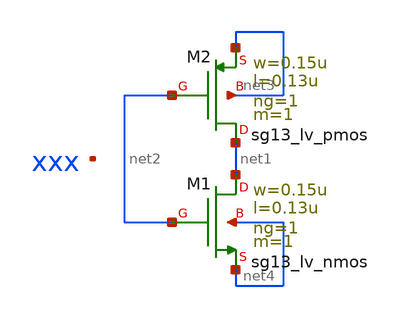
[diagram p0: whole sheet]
** sch_path: divider/inverter.sch
**.subckt inverter
XM1 net1 net2 net4 net4 sg13_lv_nmos w=0.15u l=0.13u ng=1 m=1 mm_ok=1
XM2 net1 net2 net3 net3 sg13_lv_pmos w=0.15u l=0.13u ng=1 m=1 mm_ok=1
**.ends
.end
